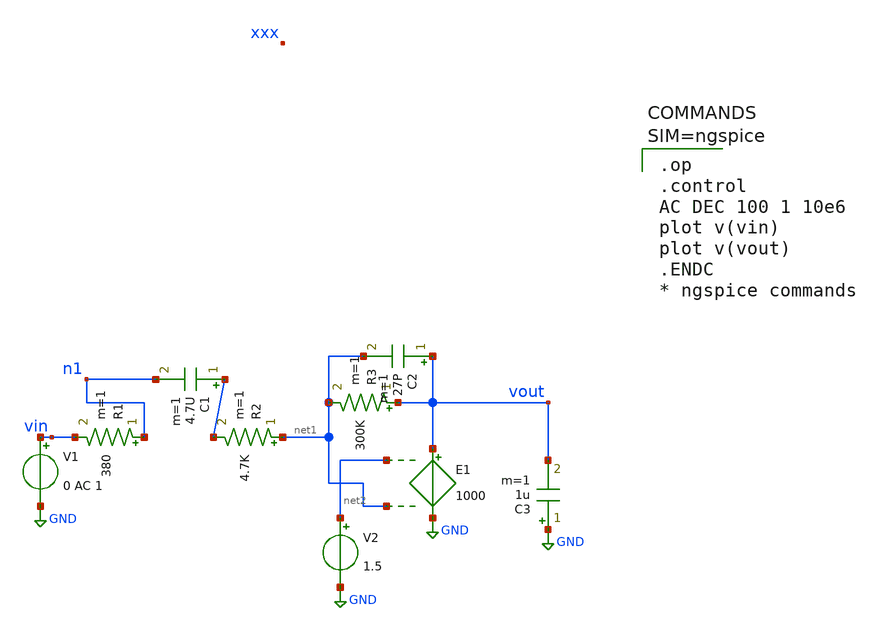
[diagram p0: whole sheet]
** sch_path: xschem/untitled.sch
**.subckt untitled
V1 vin GND 0 AC 1
R1 n1 vin 380 m=1
C1 net3 n1 4.7U m=1
R2 net1 net3 4.7K m=1
R3 vout net1 300K m=1
C2 vout net1 27P m=1
E1 vout GND net2 net1 1000
V2 net2 GND 1.5
C3 GND vout 1u m=1
**** begin user architecture code


.op
.control
AC DEC 100 1 10e6
plot v(vin)
plot v(vout)
.ENDC
* ngspice commands



**** end user architecture code
**.ends
.GLOBAL GND
.end
